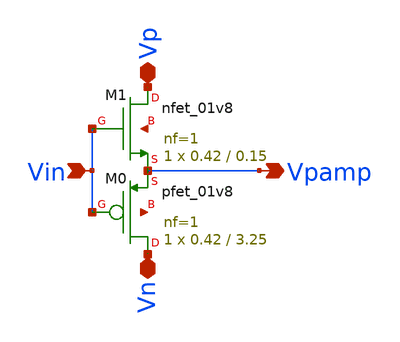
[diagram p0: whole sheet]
** sch_path: xschem/Vth_sch/Symbol/preamp_backup.sch
**.subckt preamp_backup Vin Vpamp Vp Vn
*.ipin Vin
*.opin Vpamp
*.iopin Vp
*.iopin Vn
XM1 Vp Vin Vpamp net1 sky130_fd_pr__nfet_01v8 L=0.15 W=0.42 nf=1 ad='int((nf+1)/2) * W/nf * 0.29' as='int((nf+2)/2) * W/nf * 0.29'
+ pd='2*int((nf+1)/2) * (W/nf + 0.29)' ps='2*int((nf+2)/2) * (W/nf + 0.29)' nrd='0.29 / W' nrs='0.29 / W'
+ sa=0 sb=0 sd=0 mult=1 m=1
XM0 Vn Vin Vpamp net2 sky130_fd_pr__pfet_01v8 L=3.25 W=0.42 nf=1 ad='int((nf+1)/2) * W/nf * 0.29' as='int((nf+2)/2) * W/nf * 0.29'
+ pd='2*int((nf+1)/2) * (W/nf + 0.29)' ps='2*int((nf+2)/2) * (W/nf + 0.29)' nrd='0.29 / W' nrs='0.29 / W'
+ sa=0 sb=0 sd=0 mult=1 m=1
**.ends
.end
